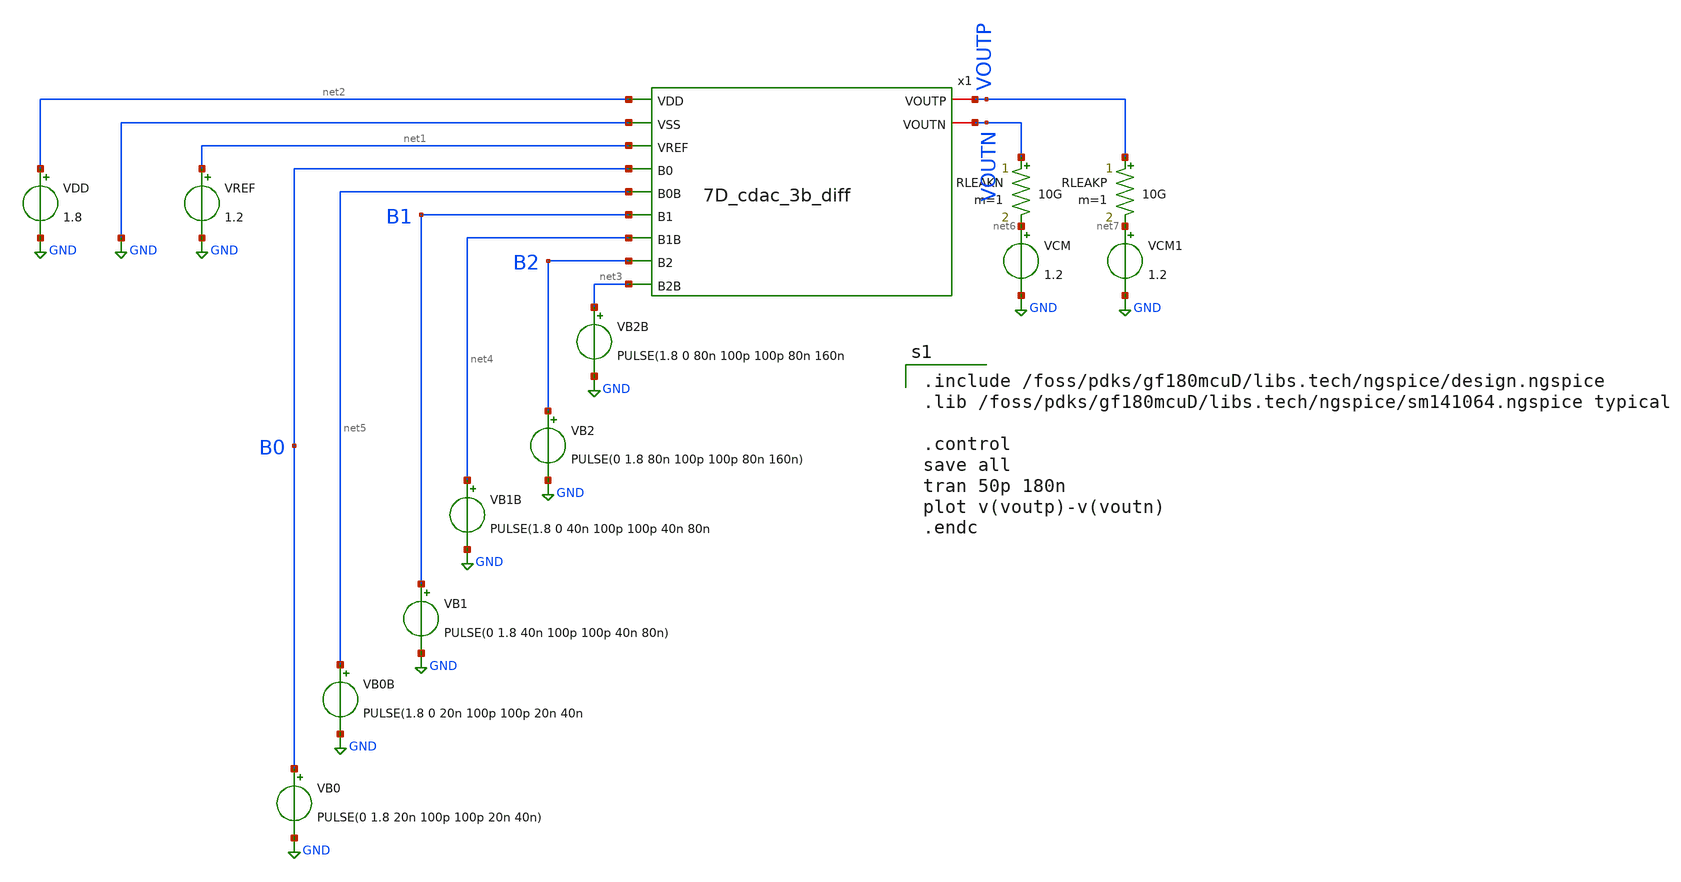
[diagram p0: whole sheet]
** sch_path: designs/libs/tb_matchmaker/tb_7D_cdac_3b_diff/tb_7D_cdac_3b_diff.sch
**.subckt tb_7D_cdac_3b_diff
VREF net1 GND 1.2
RLEAKN VOUTN net6 10G m=1
VCM net6 GND 1.2
VB2B net3 GND PULSE(1.8 0 80n 100p 100p 80n 160n
VB2 B2 GND PULSE(0 1.8 80n 100p 100p 80n 160n)
VDD net2 GND 1.8
VB1B net4 GND PULSE(1.8 0 40n 100p 100p 40n 80n
VB1 B1 GND PULSE(0 1.8 40n 100p 100p 40n 80n)
VB0B net5 GND PULSE(1.8 0 20n 100p 100p 20n 40n
VB0 B0 GND PULSE(0 1.8 20n 100p 100p 20n 40n)
x1 VOUTP net2 GND net1 B0 net5 B1 net4 B2 net3 VOUTN 7D_cdac_3b_diff
RLEAKP VOUTP net7 10G m=1
VCM1 net7 GND 1.2
**** begin user architecture code

.include /foss/pdks/gf180mcuD/libs.tech/ngspice/design.ngspice
.lib /foss/pdks/gf180mcuD/libs.tech/ngspice/sm141064.ngspice typical

.control
save all
tran 50p 180n
plot v(voutp)-v(voutn)
.endc

**** end user architecture code
**.ends
.GLOBAL GND
.end
